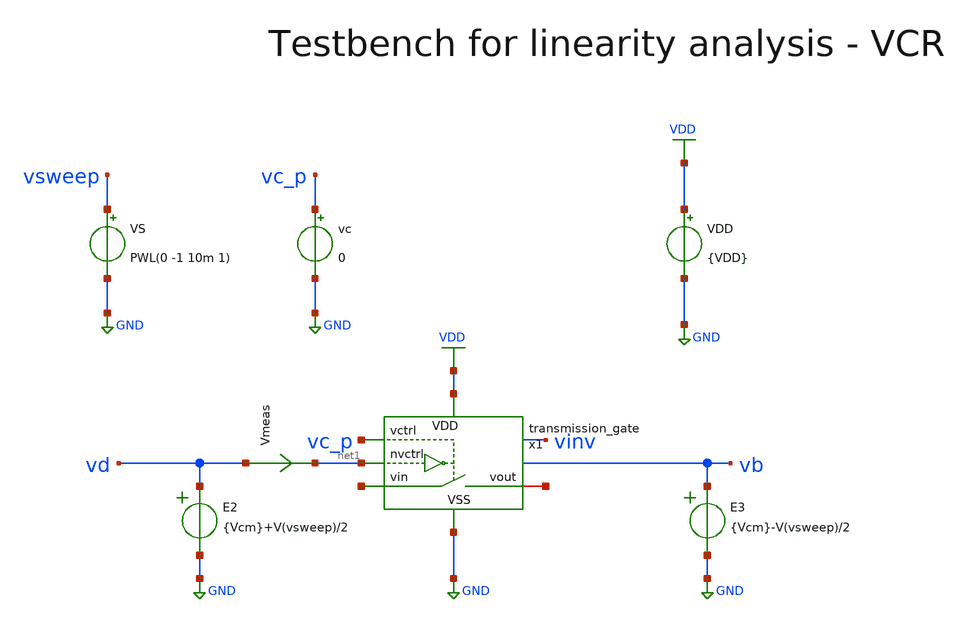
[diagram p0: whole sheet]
** sch_path: macros/heichips26_vcr/macros/switched_capacitor/testbenches/xschem/res_tb_linearity.sch
**.subckt res_tb_linearity
VDD VDD GND {VDD}
VS vsweep GND PWL(0 -1 10m 1)
Vmeas vd net1 0
.save i(vmeas)
E2 vd GND VOL=' {Vcm}+V(vsweep)/2 '
E3 vb GND VOL=' {Vcm}-V(vsweep)/2 '
vc vc_p GND 0
x1 vc_p net2 net3 net1 VDD GND transmission_gate
**** begin user architecture code

.lib cornerMOSlv.lib mos_tt
.lib cornerMOShv.lib mos_tt
.lib cornerRES.lib res_typ
.lib cornerDIO.lib dio_tt



* .include ../../../netlist/pex/inverter_magic_pex_3.spice
.param VDD=3.3
.csparam VDD=VDD
.param Vcm=VDD/2
.csparam Vcm=Vcm
.param v1=0
.csparam v1=v1
.param v2=0
.csparam v2=v2
.param temp=27
.options savecurrents klu method=gear reltol=1e-3 abstol=1e-15 gmin=1e-15
.control
let vcc = 0.0

save all
set appendwrite



repeat 5
  alter vc $&vcc

  * DC Sweep
  dc VS -3.3 3.3 10m
  remzerovec
  let vcc = vcc + 0.6
end
write @schname\.raw
set appendwrite

* Plotting
plot dc1.i(Vmeas) dc2.i(Vmeas) dc3.i(Vmeas) dc4.i(Vmeas) dc5.i(Vmeas)
*plot dc1.v(vinv) dc2.v(vinv) dc3.v(vinv) dc4.v(vinv) dc5.v(vinv)
*plot dc1.v(vc_p) dc2.v(vc_p) dc3.v(vc_p) dc4.v(vc_p) dc5.v(vc_p)
*plot dc1.v(vd) dc2.v(vd) dc3.v(vd) dc4.v(vd) dc5.v(vd)
*plot dc1.v(vb) dc2.v(vb) dc3.v(vb) dc4.v(vb) dc5.v(vb)


* Write Data
unset appendwrite
set wr_vecnames
set wr_singlescale
wrdata ../plot_simulations/data/@schname\.txt v(vc_p) dc1.v(vsweep)/(dc1.i(Vmeas))
+ dc2.v(vsweep)/(dc2.i(Vmeas)) dc3.v(vsweep)/(dc3.i(Vmeas)) dc4.v(vsweep)/(dc4.i(Vmeas)) dc5.v(vsweep)/(dc5.i(Vmeas))



*quit
.endc


**** end user architecture code
**.ends

* expanding   symbol:  transmission_gate.sym # of pins=6
** sym_path: macros/heichips26_vcr/macros/switched_capacitor/schematic/xschem/transmission_gate.sym
** sch_path: macros/heichips26_vcr/macros/switched_capacitor/schematic/xschem/transmission_gate.sch
.subckt transmission_gate vctrl vin vout nvctrl VDD VSS
*.iopin vin
*.iopin vout
*.ipin vctrl
*.ipin nvctrl
*.iopin VDD
*.iopin VSS
XM3 vout vctrl vin VSS sg13_hv_nmos w={tg_ngate_w*tg_ng} l={tg_ch_len} ng={tg_ng} m=1 mm_ok=1
XM4 vout nvctrl vin VDD sg13_hv_pmos w={tg_pgate_w*tg_ng} l={tg_ch_len} ng={tg_ng} m=1 mm_ok=1
**** begin user architecture code


.param tg_ch_len=1u
.param tg_ngate_w=2u
.param tg_pgate_w=10u
.param tg_ng=20


**** end user architecture code
.ends

.GLOBAL GND
.GLOBAL VDD
.end
